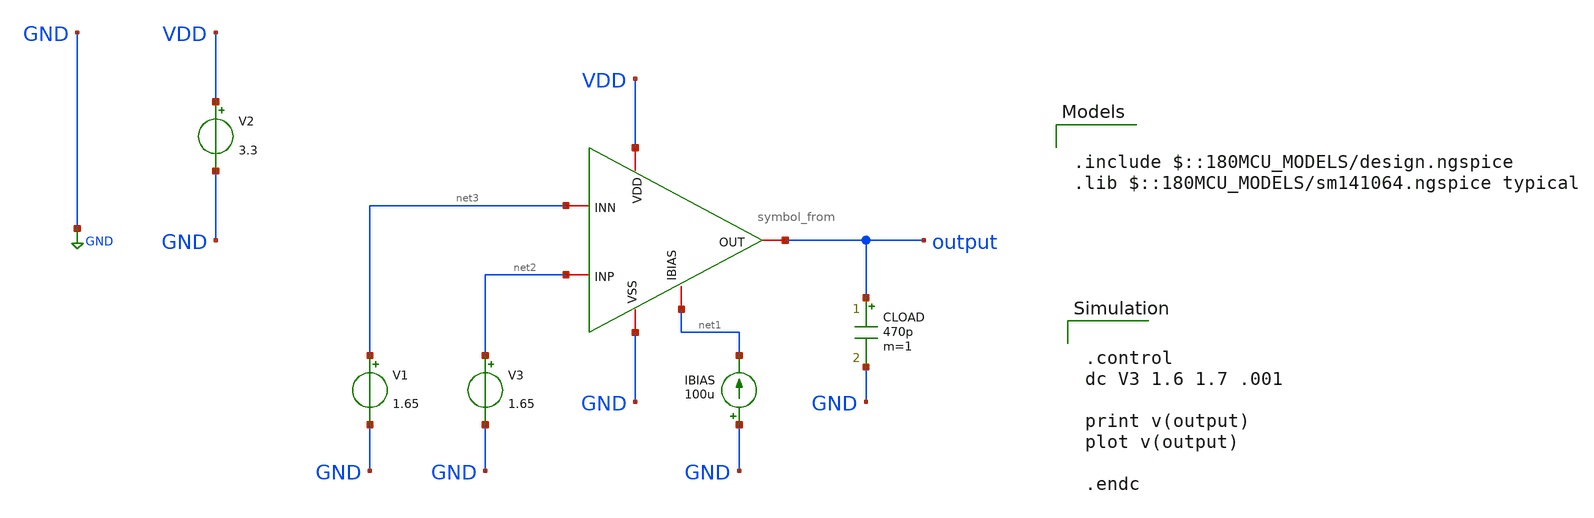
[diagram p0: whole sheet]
** sch_path: designs/libs/core_amps/ota_folded_cascode/folded_cascode_tb.sch
**.subckt folded_cascode_tb
x1 VDD output net3 net2 net1 GND symbol_from
IBIAS GND net1 100u
V2 VDD GND 3.3
CLOAD output GND 470p m=1
V1 net3 GND 1.65
V3 net2 GND 1.65
**** begin user architecture code

.include $::180MCU_MODELS/design.ngspice
.lib $::180MCU_MODELS/sm141064.ngspice typical



.control
dc V3 1.6 1.7 .001

print v(output)
plot v(output)

.endc


**** end user architecture code
**.ends

* expanding   symbol:  libs/core_amps/ota_folded_cascode/symbol_from.sym # of pins=6
** sym_path: designs/libs/core_amps/ota_folded_cascode/symbol_from.sym
** sch_path: designs/libs/core_amps/ota_folded_cascode/symbol_from.sch
.subckt symbol_from VDD OUT INN INP IBIAS VSS
*.iopin IBIAS
*.iopin INN
*.iopin INP
*.iopin OUT
*.iopin VSS
*.iopin VDD
XM1 IBIAS IBIAS VSS VSS nfet_03v3 L=.5u W=23u nf=1 ad='int((nf+1)/2) * W/nf * 0.18u' as='int((nf+2)/2) * W/nf * 0.18u'
+ pd='2*int((nf+1)/2) * (W/nf + 0.18u)' ps='2*int((nf+2)/2) * (W/nf + 0.18u)' nrd='0.18u / W' nrs='0.18u / W'
+ sa=0 sb=0 sd=0 m=1
XM2 net2 net3 VDD VDD pfet_03v3 L=.5u W=100u nf=1 ad='int((nf+1)/2) * W/nf * 0.18u' as='int((nf+2)/2) * W/nf * 0.18u'
+ pd='2*int((nf+1)/2) * (W/nf + 0.18u)' ps='2*int((nf+2)/2) * (W/nf + 0.18u)' nrd='0.18u / W' nrs='0.18u / W'
+ sa=0 sb=0 sd=0 m=1.5
XM3 OUT net3 net2 VDD pfet_03v3 L=0.5u W=78u nf=1 ad='int((nf+1)/2) * W/nf * 0.18u' as='int((nf+2)/2) * W/nf * 0.18u'
+ pd='2*int((nf+1)/2) * (W/nf + 0.18u)' ps='2*int((nf+2)/2) * (W/nf + 0.18u)' nrd='0.18u / W' nrs='0.18u / W'
+ sa=0 sb=0 sd=0 m=1
XM4 net4 net3 net1 VDD pfet_03v3 L=0.5u W=78u nf=1 ad='int((nf+1)/2) * W/nf * 0.18u' as='int((nf+2)/2) * W/nf * 0.18u'
+ pd='2*int((nf+1)/2) * (W/nf + 0.18u)' ps='2*int((nf+2)/2) * (W/nf + 0.18u)' nrd='0.18u / W' nrs='0.18u / W'
+ sa=0 sb=0 sd=0 m=1
XM5 net1 net3 VDD VDD pfet_03v3 L=.5u W=100u nf=1 ad='int((nf+1)/2) * W/nf * 0.18u' as='int((nf+2)/2) * W/nf * 0.18u'
+ pd='2*int((nf+1)/2) * (W/nf + 0.18u)' ps='2*int((nf+2)/2) * (W/nf + 0.18u)' nrd='0.18u / W' nrs='0.18u / W'
+ sa=0 sb=0 sd=0 m=1.5
XM6 net4 IBIAS net6 VSS nfet_03v3 L=0.5u W=23u nf=1 ad='int((nf+1)/2) * W/nf * 0.18u' as='int((nf+2)/2) * W/nf * 0.18u'
+ pd='2*int((nf+1)/2) * (W/nf + 0.18u)' ps='2*int((nf+2)/2) * (W/nf + 0.18u)' nrd='0.18u / W' nrs='0.18u / W'
+ sa=0 sb=0 sd=0 m=1
XM7 OUT IBIAS net5 VSS nfet_03v3 L=0.5u W=23u nf=1 ad='int((nf+1)/2) * W/nf * 0.18u' as='int((nf+2)/2) * W/nf * 0.18u'
+ pd='2*int((nf+1)/2) * (W/nf + 0.18u)' ps='2*int((nf+2)/2) * (W/nf + 0.18u)' nrd='0.18u / W' nrs='0.18u / W'
+ sa=0 sb=0 sd=0 m=1
XM8 net6 net4 VSS VSS nfet_03v3 L=.5u W=23u nf=1 ad='int((nf+1)/2) * W/nf * 0.18u' as='int((nf+2)/2) * W/nf * 0.18u'
+ pd='2*int((nf+1)/2) * (W/nf + 0.18u)' ps='2*int((nf+2)/2) * (W/nf + 0.18u)' nrd='0.18u / W' nrs='0.18u / W'
+ sa=0 sb=0 sd=0 m=2
XM9 net5 net4 VSS VSS nfet_03v3 L=.5u W=23u nf=1 ad='int((nf+1)/2) * W/nf * 0.18u' as='int((nf+2)/2) * W/nf * 0.18u'
+ pd='2*int((nf+1)/2) * (W/nf + 0.18u)' ps='2*int((nf+2)/2) * (W/nf + 0.18u)' nrd='0.18u / W' nrs='0.18u / W'
+ sa=0 sb=0 sd=0 m=2
XM10 net1 INP net7 VSS nfet_03v3 L=.5u W=11.5u nf=1 ad='int((nf+1)/2) * W/nf * 0.18u' as='int((nf+2)/2) * W/nf * 0.18u'
+ pd='2*int((nf+1)/2) * (W/nf + 0.18u)' ps='2*int((nf+2)/2) * (W/nf + 0.18u)' nrd='0.18u / W' nrs='0.18u / W'
+ sa=0 sb=0 sd=0 m=1
XM12 net7 IBIAS VSS VSS nfet_03v3 L=.5u W=23u nf=1 ad='int((nf+1)/2) * W/nf * 0.18u' as='int((nf+2)/2) * W/nf * 0.18u'
+ pd='2*int((nf+1)/2) * (W/nf + 0.18u)' ps='2*int((nf+2)/2) * (W/nf + 0.18u)' nrd='0.18u / W' nrs='0.18u / W'
+ sa=0 sb=0 sd=0 m=1
XM18 net3 net3 VDD VDD pfet_03v3 L=.5u W=78u nf=1 ad='int((nf+1)/2) * W/nf * 0.18u' as='int((nf+2)/2) * W/nf * 0.18u'
+ pd='2*int((nf+1)/2) * (W/nf + 0.18u)' ps='2*int((nf+2)/2) * (W/nf + 0.18u)' nrd='0.18u / W' nrs='0.18u / W'
+ sa=0 sb=0 sd=0 m=1
XM11 net2 INN net7 VSS nfet_03v3 L=.5u W=11.5u nf=1 ad='int((nf+1)/2) * W/nf * 0.18u' as='int((nf+2)/2) * W/nf * 0.18u'
+ pd='2*int((nf+1)/2) * (W/nf + 0.18u)' ps='2*int((nf+2)/2) * (W/nf + 0.18u)' nrd='0.18u / W' nrs='0.18u / W'
+ sa=0 sb=0 sd=0 m=1
XM13 net3 IBIAS VSS VSS nfet_03v3 L=.5u W=23u nf=1 ad='int((nf+1)/2) * W/nf * 0.18u' as='int((nf+2)/2) * W/nf * 0.18u'
+ pd='2*int((nf+1)/2) * (W/nf + 0.18u)' ps='2*int((nf+2)/2) * (W/nf + 0.18u)' nrd='0.18u / W' nrs='0.18u / W'
+ sa=0 sb=0 sd=0 m=1
.ends

.GLOBAL GND
.end
